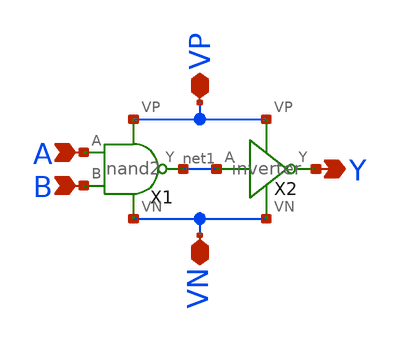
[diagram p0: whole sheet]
** sch_path: miniproject_01/xschem/and2.sch
**.subckt and2 A B VP VN Y
*.ipin A
*.ipin B
*.iopin VP
*.iopin VN
*.opin Y
X1 A net1 VP VN B nand2
X2 net1 Y VP VN inverter
**.ends

* expanding   symbol:  ENGR3426-MADVLSI/miniproject_01/xschem/nand2.sym # of pins=5
** sym_path: miniproject_01/xschem/nand2.sym
** sch_path: miniproject_01/xschem/nand2.sch
.subckt nand2 A Y VP VN B
*.opin Y
*.ipin B
*.ipin A
*.iopin VP
*.iopin VN
XM1 Y A net1 VN sky130_fd_pr__nfet_01v8 L=0.15 W=1 nf=1 ad='int((nf+1)/2) * W/nf * 0.29' as='int((nf+2)/2) * W/nf * 0.29'
+ pd='2*int((nf+1)/2) * (W/nf + 0.29)' ps='2*int((nf+2)/2) * (W/nf + 0.29)' nrd='0.29 / W' nrs='0.29 / W'
+ sa=0 sb=0 sd=0 mult=1 m=1
XM2 net1 B VN VN sky130_fd_pr__nfet_01v8 L=0.15 W=1 nf=1 ad='int((nf+1)/2) * W/nf * 0.29' as='int((nf+2)/2) * W/nf * 0.29'
+ pd='2*int((nf+1)/2) * (W/nf + 0.29)' ps='2*int((nf+2)/2) * (W/nf + 0.29)' nrd='0.29 / W' nrs='0.29 / W'
+ sa=0 sb=0 sd=0 mult=1 m=1
XM3 Y A VP VP sky130_fd_pr__pfet_01v8 L=0.15 W=1 nf=1 ad='int((nf+1)/2) * W/nf * 0.29' as='int((nf+2)/2) * W/nf * 0.29'
+ pd='2*int((nf+1)/2) * (W/nf + 0.29)' ps='2*int((nf+2)/2) * (W/nf + 0.29)' nrd='0.29 / W' nrs='0.29 / W'
+ sa=0 sb=0 sd=0 mult=1 m=1
XM4 VP B Y VP sky130_fd_pr__pfet_01v8 L=0.15 W=1 nf=1 ad='int((nf+1)/2) * W/nf * 0.29' as='int((nf+2)/2) * W/nf * 0.29'
+ pd='2*int((nf+1)/2) * (W/nf + 0.29)' ps='2*int((nf+2)/2) * (W/nf + 0.29)' nrd='0.29 / W' nrs='0.29 / W'
+ sa=0 sb=0 sd=0 mult=1 m=1
.ends


* expanding   symbol:  ENGR3426-MADVLSI/miniproject_01/xschem/inverter.sym # of pins=4
** sym_path: miniproject_01/xschem/inverter.sym
** sch_path: miniproject_01/xschem/inverter.sch
.subckt inverter A Y VP VN
*.ipin A
*.iopin VP
*.iopin VN
*.opin Y
XM1 Y A VN VN sky130_fd_pr__nfet_01v8 L=0.15 W=1 nf=1 ad='int((nf+1)/2) * W/nf * 0.29' as='int((nf+2)/2) * W/nf * 0.29'
+ pd='2*int((nf+1)/2) * (W/nf + 0.29)' ps='2*int((nf+2)/2) * (W/nf + 0.29)' nrd='0.29 / W' nrs='0.29 / W'
+ sa=0 sb=0 sd=0 mult=1 m=1
XM2 Y A VP VP sky130_fd_pr__pfet_01v8 L=0.15 W=1 nf=1 ad='int((nf+1)/2) * W/nf * 0.29' as='int((nf+2)/2) * W/nf * 0.29'
+ pd='2*int((nf+1)/2) * (W/nf + 0.29)' ps='2*int((nf+2)/2) * (W/nf + 0.29)' nrd='0.29 / W' nrs='0.29 / W'
+ sa=0 sb=0 sd=0 mult=1 m=1
.ends

.end
